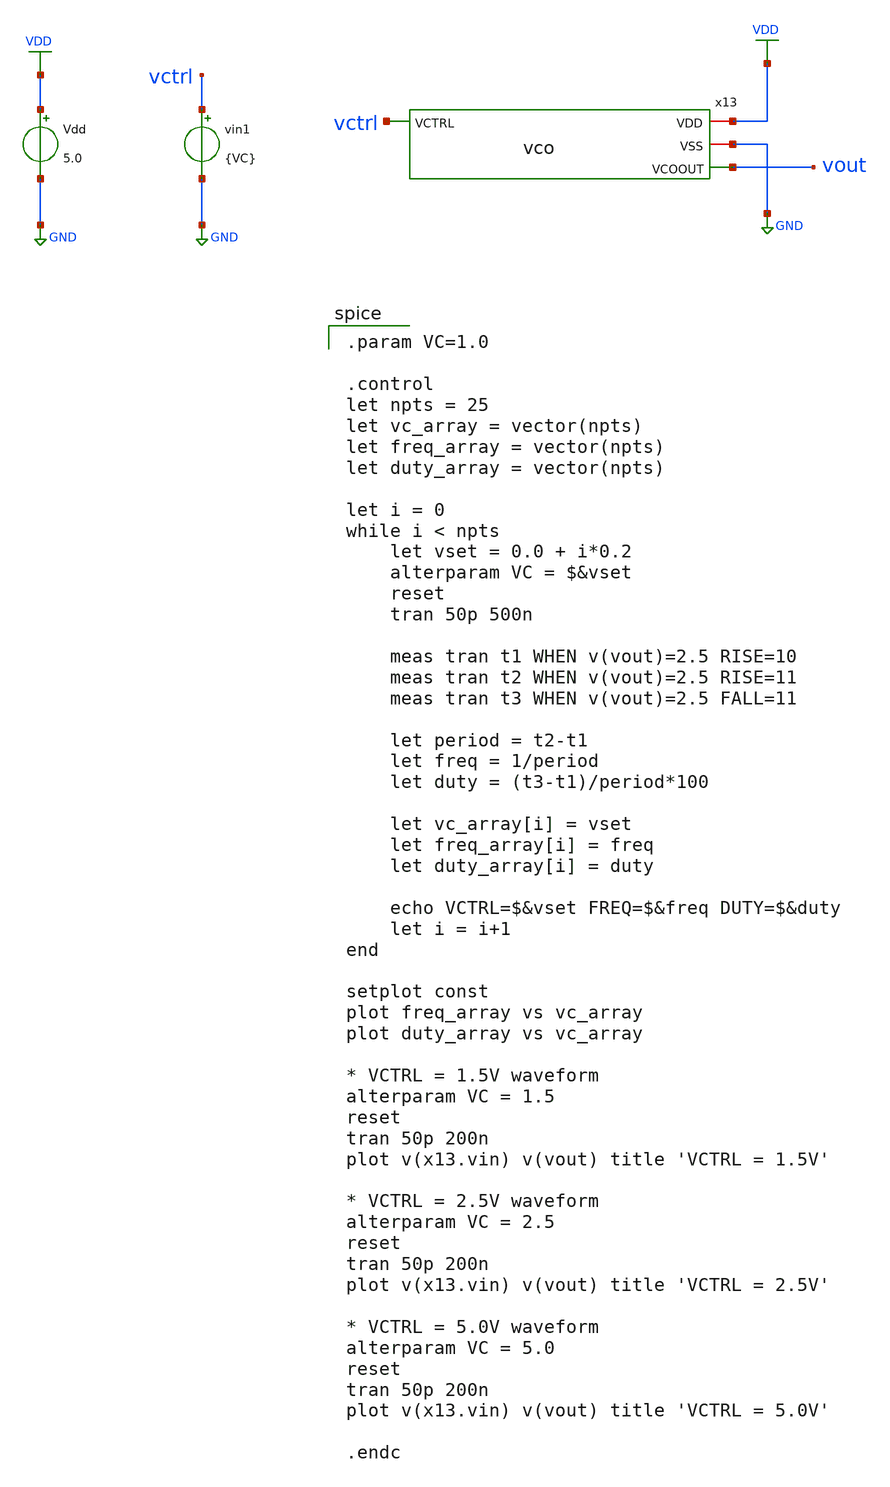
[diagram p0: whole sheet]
** sch_path: src/vco_tb.sch
**.subckt vco_tb
Vdd VDD GND 5.0
vin1 vctrl GND {VC}
x13 vctrl VDD GND vout vco
**** begin user architecture code

.param VC=1.0

.control
let npts = 25
let vc_array = vector(npts)
let freq_array = vector(npts)
let duty_array = vector(npts)

let i = 0
while i < npts
    let vset = 0.0 + i*0.2
    alterparam VC = $&vset
    reset
    tran 50p 500n

    meas tran t1 WHEN v(vout)=2.5 RISE=10
    meas tran t2 WHEN v(vout)=2.5 RISE=11
    meas tran t3 WHEN v(vout)=2.5 FALL=11

    let period = t2-t1
    let freq = 1/period
    let duty = (t3-t1)/period*100

    let vc_array[i] = vset
    let freq_array[i] = freq
    let duty_array[i] = duty

    echo VCTRL=$&vset FREQ=$&freq DUTY=$&duty
    let i = i+1
end

setplot const
plot freq_array vs vc_array
plot duty_array vs vc_array

* VCTRL = 1.5V waveform
alterparam VC = 1.5
reset
tran 50p 200n
plot v(x13.vin) v(vout) title 'VCTRL = 1.5V'

* VCTRL = 2.5V waveform
alterparam VC = 2.5
reset
tran 50p 200n
plot v(x13.vin) v(vout) title 'VCTRL = 2.5V'

* VCTRL = 5.0V waveform
alterparam VC = 5.0
reset
tran 50p 200n
plot v(x13.vin) v(vout) title 'VCTRL = 5.0V'

.endc



 .include $::LIB/ip62_models
**** end user architecture code
**.ends
.GLOBAL VDD
.GLOBAL GND
.end
